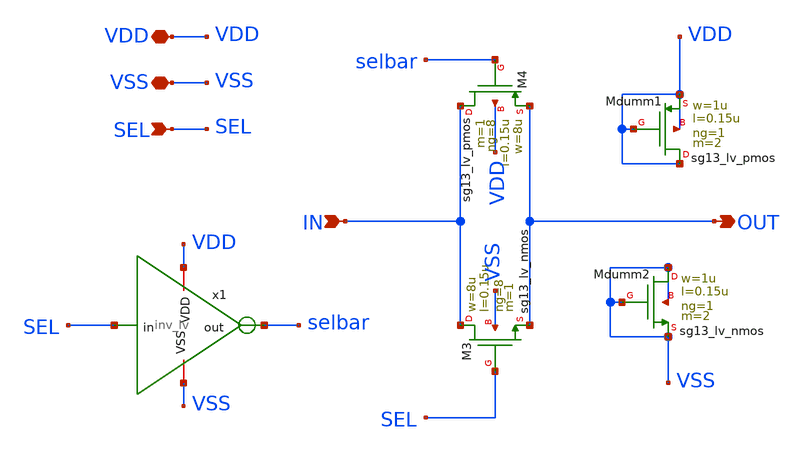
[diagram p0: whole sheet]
** sch_path: xschem/tg_lv.sch
**.subckt tg_lv IN VDD VSS OUT SEL
*.ipin IN
*.iopin VDD
*.iopin VSS
*.opin OUT
*.ipin SEL
x1 VDD SEL selbar VSS inv_lv
XM3 IN SEL OUT VSS sg13_lv_nmos w=8u l=0.15u ng=8 m=1 mm_ok=1
XM4 IN selbar OUT VDD sg13_lv_pmos w=8u l=0.15u ng=8 m=1 mm_ok=1
XMdumm1 VDD VDD VDD VDD sg13_lv_pmos w=1u l=0.15u ng=1 m=2 mm_ok=1
XMdumm2 VSS VSS VSS VSS sg13_lv_nmos w=1u l=0.15u ng=1 m=2 mm_ok=1
**.ends

* expanding   symbol:  inv_lv.sym # of pins=4
** sym_path: inv_lv.sym
** sch_path: inv_lv.sch
.subckt inv_lv VDD in out VSS
*.ipin in
*.opin out
*.iopin VDD
*.iopin VSS
XM3 out in VDD VDD sg13_lv_pmos w=1u l=0.15u ng=1 m=1 mm_ok=1
XM4 out in VSS VSS sg13_lv_nmos w=1u l=0.15u ng=1 m=1 mm_ok=1
XMdumm1 VDD VDD VDD VDD sg13_lv_pmos w=1u l=0.15u ng=1 m=2 mm_ok=1
XMdumm2 VSS VSS VSS VSS sg13_lv_nmos w=1u l=0.15u ng=1 m=2 mm_ok=1
.ends

.end
